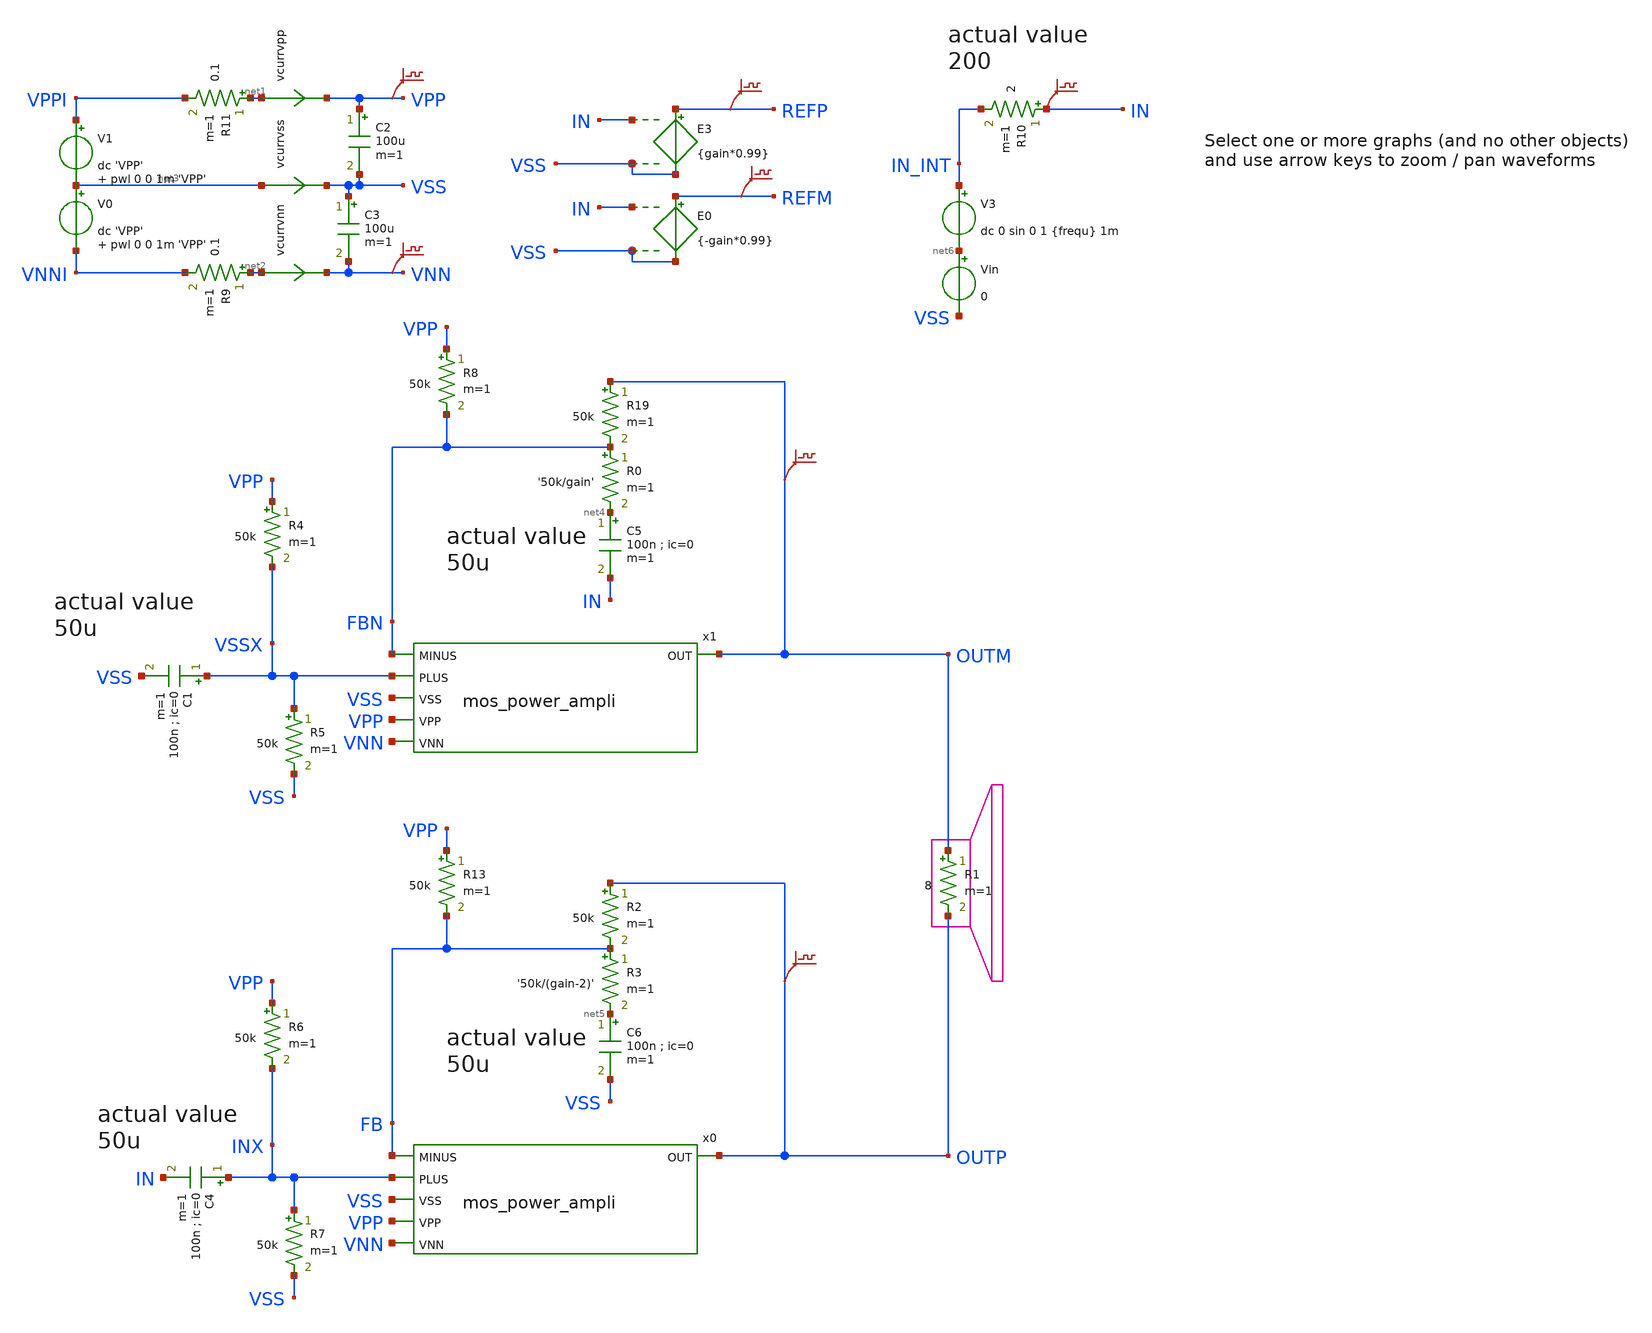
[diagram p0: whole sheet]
** sch_path: xschem-src/xschem_library/examples/poweramp.sch
* Copyright (C) 1998-2026 Stefan Frederik Schippers
* This program is free software; you can redistribute it and/or modify
* it under the terms of the GNU General Public License as published by
* the Free Software Foundation; either version 2 of the License, or
* (at your option) any later version.
* This program is distributed in the hope that it will be useful,
* but WITHOUT ANY WARRANTY; without even the implied warranty of
* MERCHANTABILITY or FITNESS FOR A PARTICULAR PURPOSE.  See the
* GNU General Public License for more details.
* You should have received a copy of the GNU General Public License
* along with this program; if not, write to the Free Software
**.subckt poweramp
V1 VPPI net3 dc 'VPP' pwl 0 0 1m 'VPP'
V0 net3 VNNI dc 'VPP' pwl 0 0 1m 'VPP'
R1 OUTM OUTP 8 m=1
E3 REFP VSS IN VSS {gain*0.99}
C3 VSS VNN 100u m=1
R11 net1 VPPI 0.1 m=1
R9 net2 VNNI 0.1 m=1
R19 OUTM FBN 50k m=1
R0 FBN net4 '50k/gain' m=1
x1 FBN VSSX VSS OUTM VPP VNN mos_power_ampli
x0 FB INX VSS OUTP VPP VNN mos_power_ampli
R6 VPP INX 50k m=1
R7 INX VSS 50k m=1
E0 REFM VSS IN VSS {-gain*0.99}
C5 net4 IN 100n ; ic=0 m=1
C6 net5 VSS 100n ; ic=0 m=1
R2 OUTP FB 50k m=1
R3 FB net5 '50k/(gain-2)' m=1
V3 IN_INT net6 dc 0 sin 0 1 {frequ} 1m
R4 VPP VSSX 50k m=1
R5 VSSX VSS 50k m=1
R8 VPP FBN 50k m=1
C4 INX IN 100n ; ic=0 m=1
C1 VSSX VSS 100n ; ic=0 m=1
R10 IN IN_INT 2 m=1
R13 VPP FB 50k m=1
Vin net6 VSS 0
vcurrvpp net1 VPP 0
.save i(vcurrvpp)
vcurrvnn net2 VNN 0
.save i(vcurrvnn)
vcurrvss net3 VSS 0
.save i(vcurrvss)
C2 VPP VSS 100u m=1
.save v(outm)
.save v(outp)
.save v(refp)
.save v(refm)
.save v(in)
.save v(vpp)
.save v(vnn)
**** begin user architecture code



.option ITL4=20000 ITL5=0
vvss vss 0 dc 0
.param VPP=50
.temp 30
.param frequ=15k
.param gain=45
.option savecurrents

** models are generally not free: you must download
** SPICE models for active devices and put them  into the below
** referenced file in simulation directory.
.include "models_poweramp.txt"
.control
save all
op
write poweramp.raw
set appendwrite
tran  2e-7 0.025 uic
* .FOUR 20k v(outm,outp)
* .probe i(*)
save p(r*) p(v*)
write poweramp.raw
quit 0
.endc






**** end user architecture code
**.ends

* expanding   symbol:  mos_power_ampli.sym # of pins=6
** sym_path: xschem-src/xschem_library/examples/mos_power_ampli.sym
** sch_path: xschem-src/xschem_library/examples/mos_power_ampli.sch
.subckt mos_power_ampli MINUS PLUS VSS OUT VPP VNN
*.ipin PLUS
*.ipin VNN
*.opin OUT
*.ipin MINUS
*.ipin VSS
*.ipin VPP
xm2 net1 GB SB irf540 m=1
R7 GB SB 320 m=1
xm1 VPP GA SA irf540 m=1
R0 GA SA 320 m=1
R2 VPP E2 50 m=1
R3 VBOOST E1 50 m=1
Q5 C5 PLUS E9 q2n2222 area=1 m=1
Q4 net8 net2 E4 q2n2907p area=1 m=1
R9 VBOOST E4 50 m=1
Q6 C6 C2 net5 q2n2907p area=1 m=1
R4 VPP E6 50 m=1
vd OUTI net1 0
.save i(vd)
vu SA OUTI 0
.save i(vu)
Q1 net2 net2 E1 q2n2907p area=1 m=1
Q2 C2 C2 net4 q2n2907p area=1 m=1
Q9 C9 MINUS E9 q2n2222 area=1 m=1
R11 GB net6 1000 m=1
Q8 C8 VSS E8 q2n2907p area=1 m=1
C12 VBOOST net3 40u m=1
D0 VPP VBOOST d1n4148 area=1
R18 net3 OUTI 200 m=1
D1 VPP VBOOST d1n758
R14 B1 net7 4k m=1
Q11 GA B1 E11 q2n2907p area=1 m=1
R15 VBOOST B1 4k m=1
R5 E9 net9 40 m=1
R6 net9 net10 40 m=1
D2 VSS B3 1N746
Q3 C3 B3 E3 q2n2222 area=1 m=1
R1 VPP B3 7k m=1
R10 E3 VSS 110 m=1
C3 B3 VSS 100n m=1
R12 C6 E8 400 m=1
R13 C2 C9 300 m=1
Q7 C7 C9 C5 q2n2222 area=1 m=1
v0 SB VNN 0
.save i(v0)
v1 E6 net5 0
.save i(v1)
v2 E2 net4 0
.save i(v2)
v3 net10 C3 0
.save i(v3)
v4 C8 net6 0
.save i(v4)
v5 net7 OUTI 0
.save i(v5)
v6 net2 C7 0
.save i(v6)
v7 net8 E11 0
.save i(v7)
.save v(gb)
.save v(sb)
.save v(ga)
.save v(sa)
v8 OUTI OUT 0
.save i(v8)
.save v(ga)
.save v(gb)
.save v(c2)
.save v(net2)
.save v(c7)
.save v(vboost)
.save v(outi)
.ends

.end
